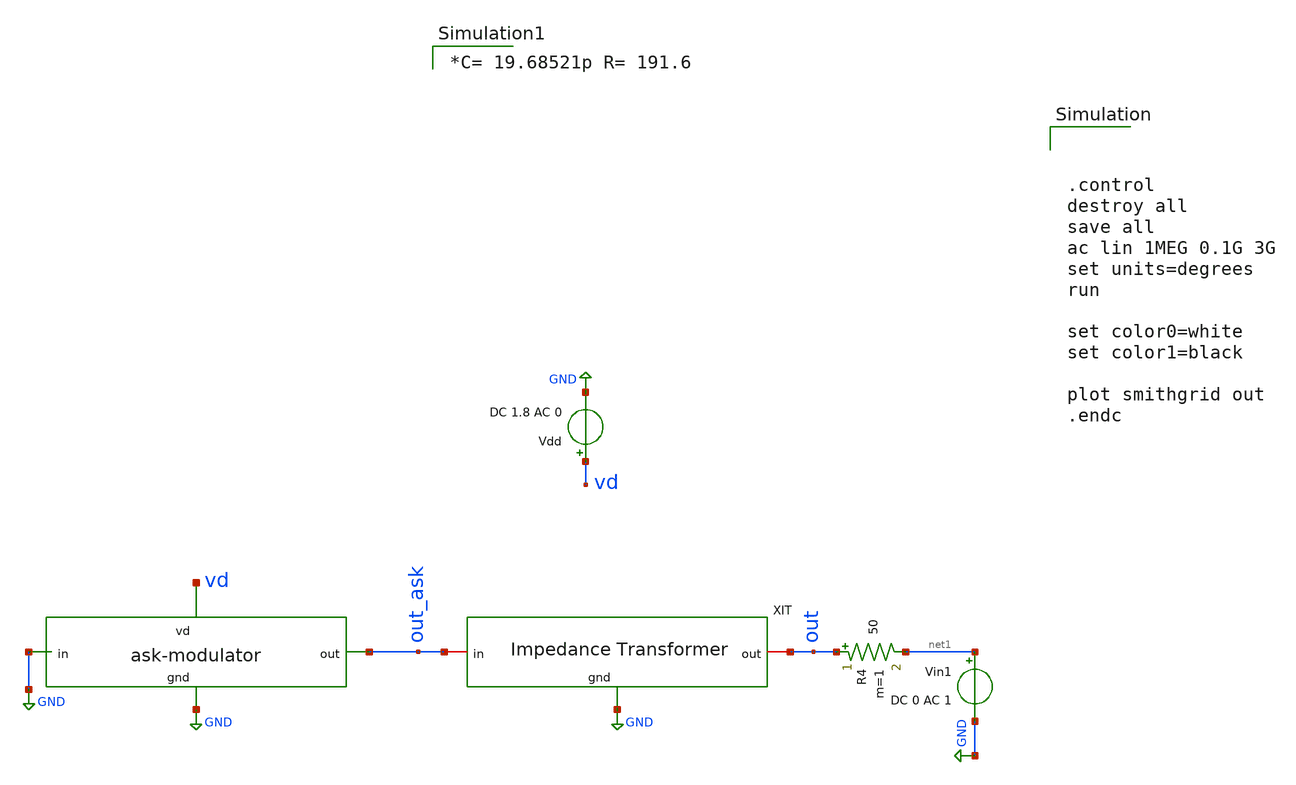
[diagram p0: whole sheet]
** sch_path: impedance-transformer/xschem/impedance-transformer_tb-ac2.sch
**.subckt impedance-transformer_tb-ac2
Vin1 net1 GND DC 0 AC 1
R4 out net1 50 m=1
x2 out_ask out GND impedance-transformer
x1 vd out_ask GND GND ask-modulator
Vdd vd GND DC 1.8 AC 0
**** begin user architecture code



.control
destroy all
save all
ac lin 1MEG 0.1G 3G
set units=degrees
run

set color0=white
set color1=black

plot smithgrid out
.endc

 .lib $::SKYWATER_MODELS/sky130.lib.spice tt
.include $::SKYWATER_STDCELLS/sky130_fd_sc_hd.spice


*C= 19.68521p R= 191.6

**** end user architecture code
**.ends
.GLOBAL GND
.end
